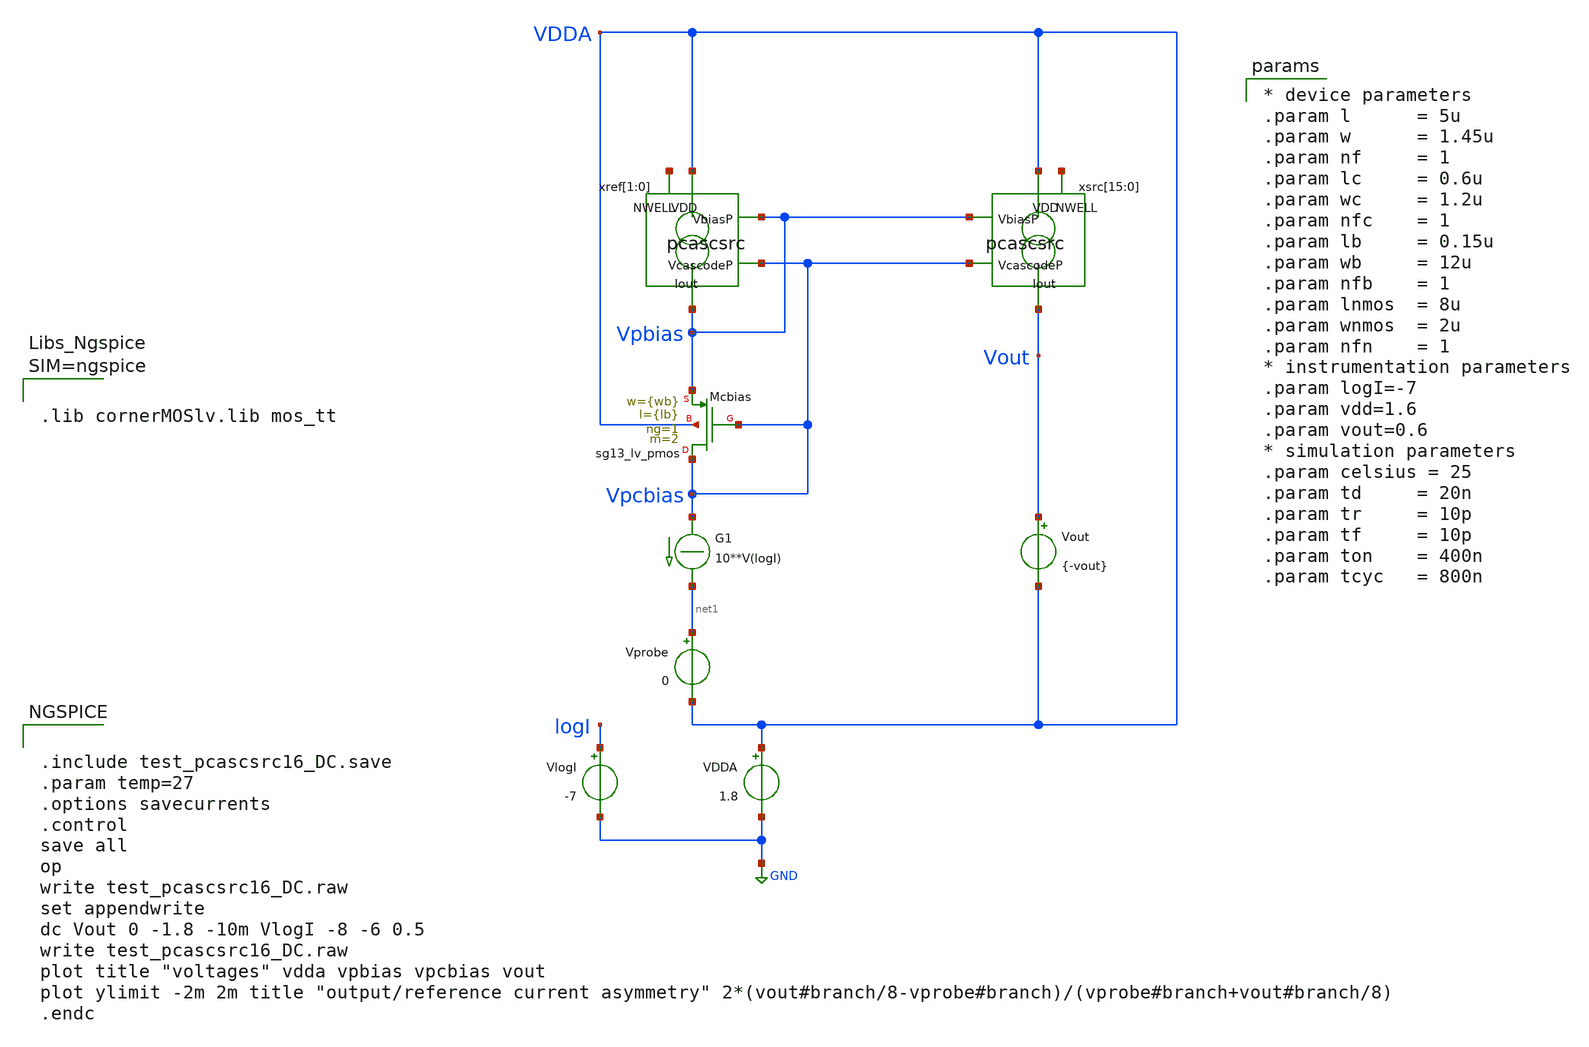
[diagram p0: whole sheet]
** sch_path: xschem/test_pcascsrc16_DC.sch
**.subckt test_pcascsrc16_DC
Vout Vout VDDA {-vout}
.save i(vout)
Vprobe net1 VDDA 0
.save i(vprobe)
G1 Vpcbias net1 CUR=' 10**V(logI) '
VlogI logI GND -7
.save i(vlogi)
xref[1] VDDA Vpbias Vpcbias Vpbias net2[1] pcascsrc
xref[0] VDDA Vpbias Vpcbias Vpbias net2[0] pcascsrc
xsrc[15] VDDA Vpbias Vpcbias Vout net3[15] pcascsrc
xsrc[14] VDDA Vpbias Vpcbias Vout net3[14] pcascsrc
xsrc[13] VDDA Vpbias Vpcbias Vout net3[13] pcascsrc
xsrc[12] VDDA Vpbias Vpcbias Vout net3[12] pcascsrc
xsrc[11] VDDA Vpbias Vpcbias Vout net3[11] pcascsrc
xsrc[10] VDDA Vpbias Vpcbias Vout net3[10] pcascsrc
xsrc[9] VDDA Vpbias Vpcbias Vout net3[9] pcascsrc
xsrc[8] VDDA Vpbias Vpcbias Vout net3[8] pcascsrc
xsrc[7] VDDA Vpbias Vpcbias Vout net3[7] pcascsrc
xsrc[6] VDDA Vpbias Vpcbias Vout net3[6] pcascsrc
xsrc[5] VDDA Vpbias Vpcbias Vout net3[5] pcascsrc
xsrc[4] VDDA Vpbias Vpcbias Vout net3[4] pcascsrc
xsrc[3] VDDA Vpbias Vpcbias Vout net3[3] pcascsrc
xsrc[2] VDDA Vpbias Vpcbias Vout net3[2] pcascsrc
xsrc[1] VDDA Vpbias Vpcbias Vout net3[1] pcascsrc
xsrc[0] VDDA Vpbias Vpcbias Vout net3[0] pcascsrc
VDDA VDDA GND 1.8
.save i(vdda)
XMcbias Vpcbias Vpcbias Vpbias VDDA sg13_lv_pmos w={wb} l={lb} ng=1 m=2 mm_ok=1
**** begin user architecture code


.include test_pcascsrc16_DC.save
.param temp=27
.options savecurrents
.control
save all
op
write test_pcascsrc16_DC.raw
set appendwrite
dc Vout 0 -1.8 -10m VlogI -8 -6 0.5
write test_pcascsrc16_DC.raw
plot title "voltages" vdda vpbias vpcbias vout
plot ylimit -2m 2m title "output/reference current asymmetry"
+ 2*(vout#branch/8-vprobe#branch)/(vprobe#branch+vout#branch/8)
.endc





.lib cornerMOSlv.lib mos_tt




* device parameters
.param l      = 5u
.param w      = 1.45u
.param nf     = 1
.param lc     = 0.6u
.param wc     = 1.2u
.param nfc    = 1
.param lb     = 0.15u
.param wb     = 12u
.param nfb    = 1
.param lnmos  = 8u
.param wnmos  = 2u
.param nfn    = 1
* instrumentation parameters
.param logI=-7
.param vdd=1.6
.param vout=0.6
* simulation parameters
.param celsius = 25
.param td     = 20n
.param tr     = 10p
.param tf     = 10p
.param ton    = 400n
.param tcyc   = 800n


**** end user architecture code
**.ends

* expanding   symbol:  pcascsrc.sym # of pins=5
** sym_path: xschem/pcascsrc.sym
** sch_path: xschem/pcascsrc.sch
.subckt pcascsrc VDD VbiasP VcascodeP Iout NWELL
*.ipin VcascodeP
*.ipin VbiasP
*.opin Iout
*.ipin VDD
*.iopin NWELL
XMsrc drain VbiasP VDD NWELL sg13_lv_pmos w=0.74u l=2u ng=1 m=1 mm_ok=1
XMcasc Iout VcascodeP drain NWELL sg13_lv_pmos w=0.3u l=0.3u ng=1 m=1 mm_ok=1
.ends

.GLOBAL GND
.end
